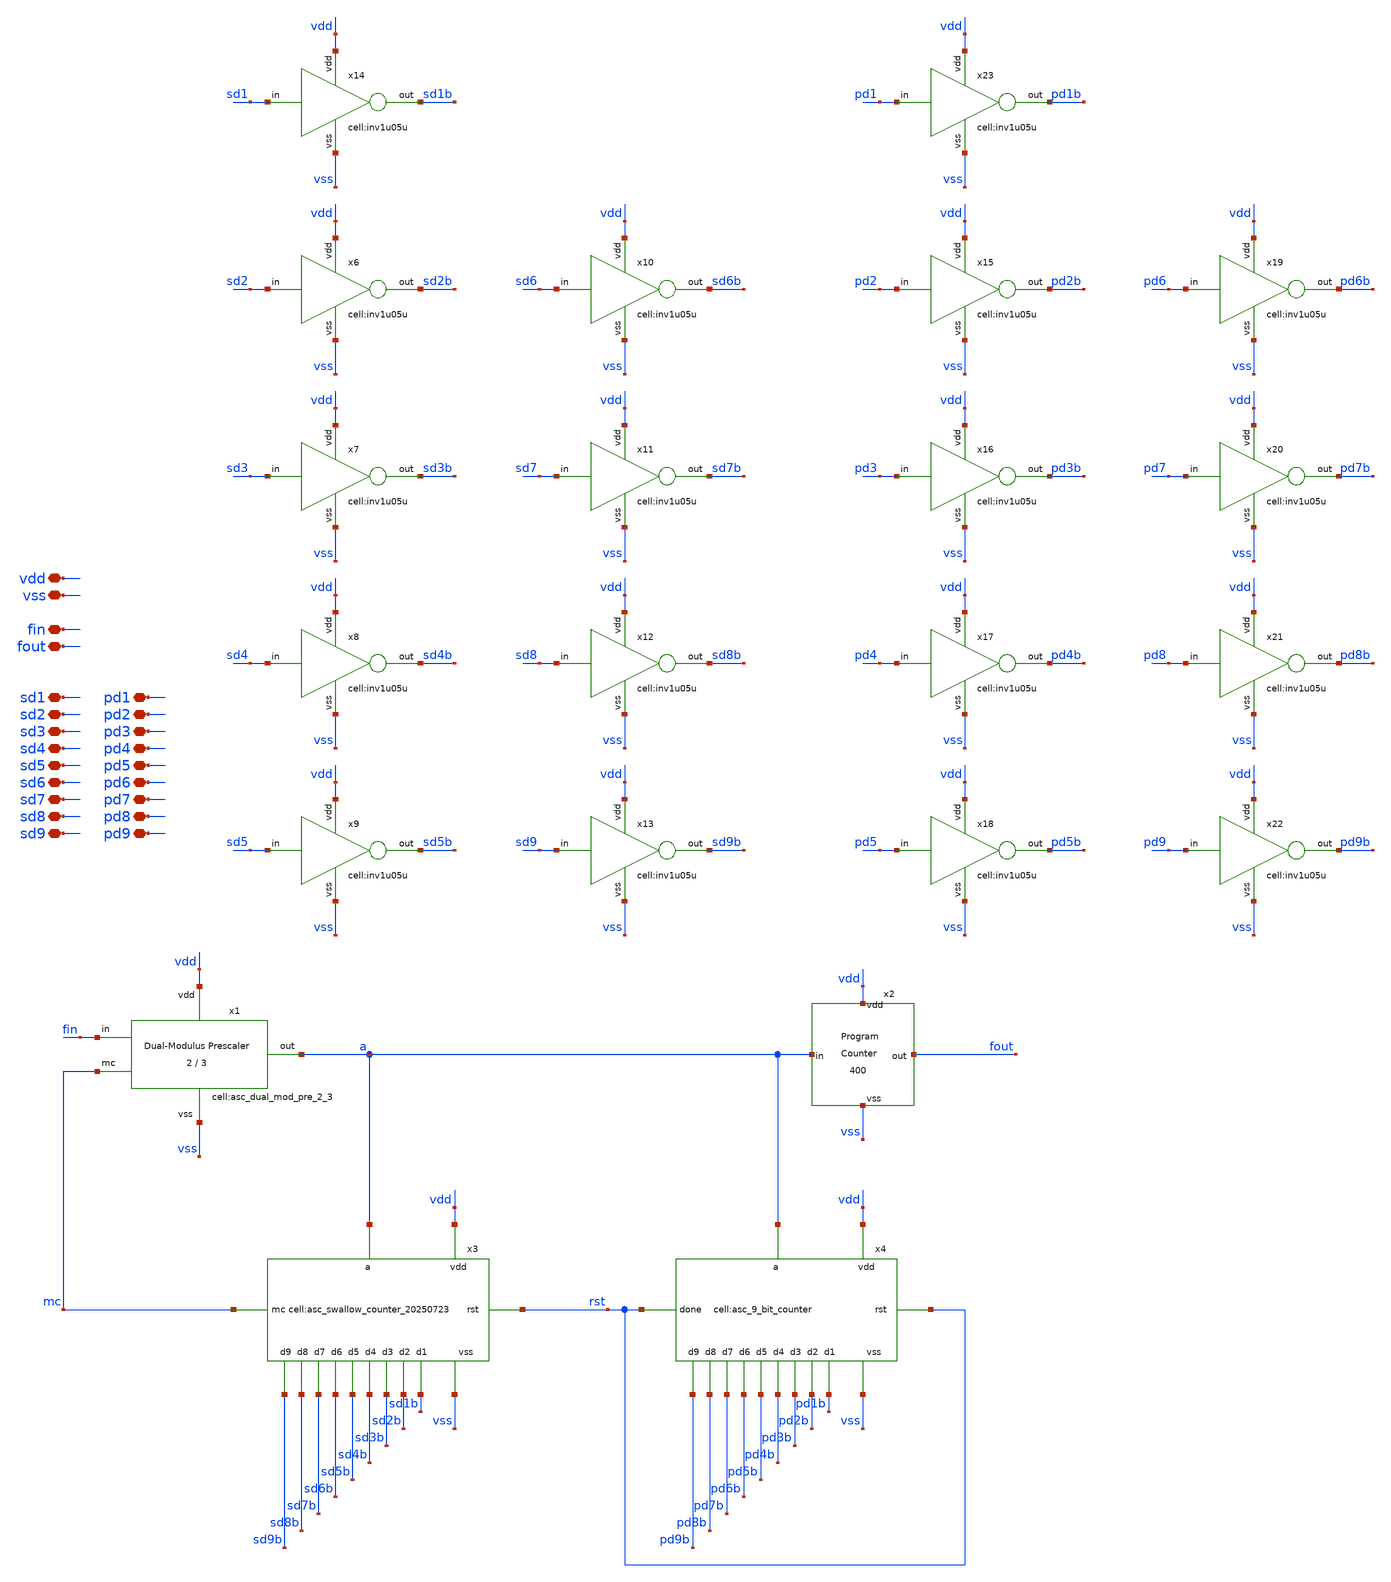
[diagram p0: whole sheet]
** sch_path: designs/libs/xp_core_analog/asc_FM_pulse_swallow_divider/asc_FM_pulse_swallow_divider.sch
**.subckt asc_FM_pulse_swallow_divider vdd vss sd2 sd1 sd3 sd5 sd4 sd6 sd8 sd7 sd9 fin fout pd2 pd1
*+ pd3 pd5 pd4 pd6 pd8 pd7 pd9
*.iopin vdd
*.iopin vss
*.iopin sd2
*.iopin sd1
*.iopin sd3
*.iopin sd5
*.iopin sd4
*.iopin sd6
*.iopin sd8
*.iopin sd7
*.iopin sd9
*.iopin fin
*.iopin fout
*.iopin pd2
*.iopin pd1
*.iopin pd3
*.iopin pd5
*.iopin pd4
*.iopin pd6
*.iopin pd8
*.iopin pd7
*.iopin pd9
x1 vdd vss a fin mc asc_dual_mod_pre_2_3
x2 a fout vdd vss asc_program_counter_400
x4 rst pd9b pd8b pd7b pd6b pd5b pd4b pd3b pd2b pd1b vss rst vdd a asc_9_bit_counter
x6 sd2 vdd sd2b vss inv1u05u
x7 sd3 vdd sd3b vss inv1u05u
x8 sd4 vdd sd4b vss inv1u05u
x9 sd5 vdd sd5b vss inv1u05u
x10 sd6 vdd sd6b vss inv1u05u
x11 sd7 vdd sd7b vss inv1u05u
x12 sd8 vdd sd8b vss inv1u05u
x13 sd9 vdd sd9b vss inv1u05u
x14 sd1 vdd sd1b vss inv1u05u
x15 pd2 vdd pd2b vss inv1u05u
x16 pd3 vdd pd3b vss inv1u05u
x17 pd4 vdd pd4b vss inv1u05u
x18 pd5 vdd pd5b vss inv1u05u
x19 pd6 vdd pd6b vss inv1u05u
x20 pd7 vdd pd7b vss inv1u05u
x21 pd8 vdd pd8b vss inv1u05u
x22 pd9 vdd pd9b vss inv1u05u
x23 pd1 vdd pd1b vss inv1u05u
x3 mc sd9b sd8b sd7b sd6b sd5b sd4b sd3b sd2b sd1b vss rst vdd a asc_swallow_counter_20250723
**.ends
.end
